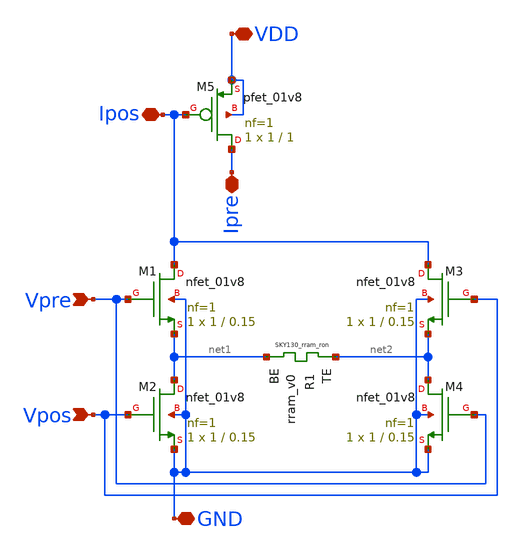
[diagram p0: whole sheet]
** sch_path: synapse/4T1R.sch
**.subckt 4T1R Vpre Vpos GND Ipre Ipos VDD
*.ipin Vpre
*.ipin Vpos
*.iopin GND
*.iopin Ipre
*.iopin Ipos
*.iopin VDD
XM1 Ipos Vpre net1 GND sky130_fd_pr__nfet_01v8 L=0.15 W=1 nf=1 ad='int((nf+1)/2) * W/nf * 0.29' as='int((nf+2)/2) * W/nf * 0.29'
+ pd='2*int((nf+1)/2) * (W/nf + 0.29)' ps='2*int((nf+2)/2) * (W/nf + 0.29)' nrd='0.29 / W' nrs='0.29 / W'
+ sa=0 sb=0 sd=0 mult=1 m=1
XR1 net2 net1 rram_v0
XM2 net1 Vpos GND GND sky130_fd_pr__nfet_01v8 L=0.15 W=1 nf=1 ad='int((nf+1)/2) * W/nf * 0.29' as='int((nf+2)/2) * W/nf * 0.29'
+ pd='2*int((nf+1)/2) * (W/nf + 0.29)' ps='2*int((nf+2)/2) * (W/nf + 0.29)' nrd='0.29 / W' nrs='0.29 / W'
+ sa=0 sb=0 sd=0 mult=1 m=1
XM3 Ipos Vpos net2 GND sky130_fd_pr__nfet_01v8 L=0.15 W=1 nf=1 ad='int((nf+1)/2) * W/nf * 0.29' as='int((nf+2)/2) * W/nf * 0.29'
+ pd='2*int((nf+1)/2) * (W/nf + 0.29)' ps='2*int((nf+2)/2) * (W/nf + 0.29)' nrd='0.29 / W' nrs='0.29 / W'
+ sa=0 sb=0 sd=0 mult=1 m=1
XM4 net2 Vpre GND GND sky130_fd_pr__nfet_01v8 L=0.15 W=1 nf=1 ad='int((nf+1)/2) * W/nf * 0.29' as='int((nf+2)/2) * W/nf * 0.29'
+ pd='2*int((nf+1)/2) * (W/nf + 0.29)' ps='2*int((nf+2)/2) * (W/nf + 0.29)' nrd='0.29 / W' nrs='0.29 / W'
+ sa=0 sb=0 sd=0 mult=1 m=1
XM5 Ipre Ipos VDD VDD sky130_fd_pr__pfet_01v8 L=1 W=1 nf=1 ad='int((nf+1)/2) * W/nf * 0.29' as='int((nf+2)/2) * W/nf * 0.29'
+ pd='2*int((nf+1)/2) * (W/nf + 0.29)' ps='2*int((nf+2)/2) * (W/nf + 0.29)' nrd='0.29 / W' nrs='0.29 / W'
+ sa=0 sb=0 sd=0 mult=1 m=1
**.ends
.end
